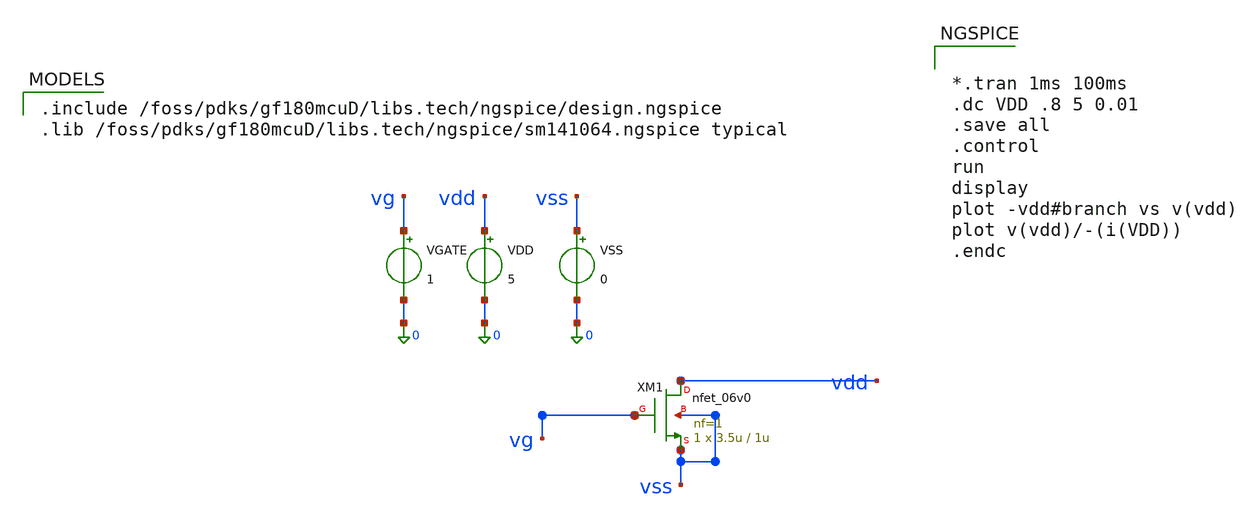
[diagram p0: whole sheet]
** sch_path: activities/opamp3An/NMOS_Linearity_Check.sch
**.subckt NMOS_Linearity_Check
VGATE vg 0 1
VDD vdd 0 5
VSS vss 0 0
XM1 vdd vg vss vss nfet_06v0 L=1u W=3.5u nf=1 ad='int((nf+1)/2) * W/nf * 0.18u' as='int((nf+2)/2) * W/nf * 0.18u'
+ pd='2*int((nf+1)/2) * (W/nf + 0.18u)' ps='2*int((nf+2)/2) * (W/nf + 0.18u)' nrd='0.18u / W' nrs='0.18u / W'
+ sa=0 sb=0 sd=0 m=1
**** begin user architecture code

.include /foss/pdks/gf180mcuD/libs.tech/ngspice/design.ngspice
.lib /foss/pdks/gf180mcuD/libs.tech/ngspice/sm141064.ngspice typical



*.tran 1ms 100ms
.dc VDD .8 5 0.01
.save all
.control
run
display
plot -vdd#branch vs v(vdd)
plot v(vdd)/-(i(VDD))
.endc


**** end user architecture code
**.ends
.end
